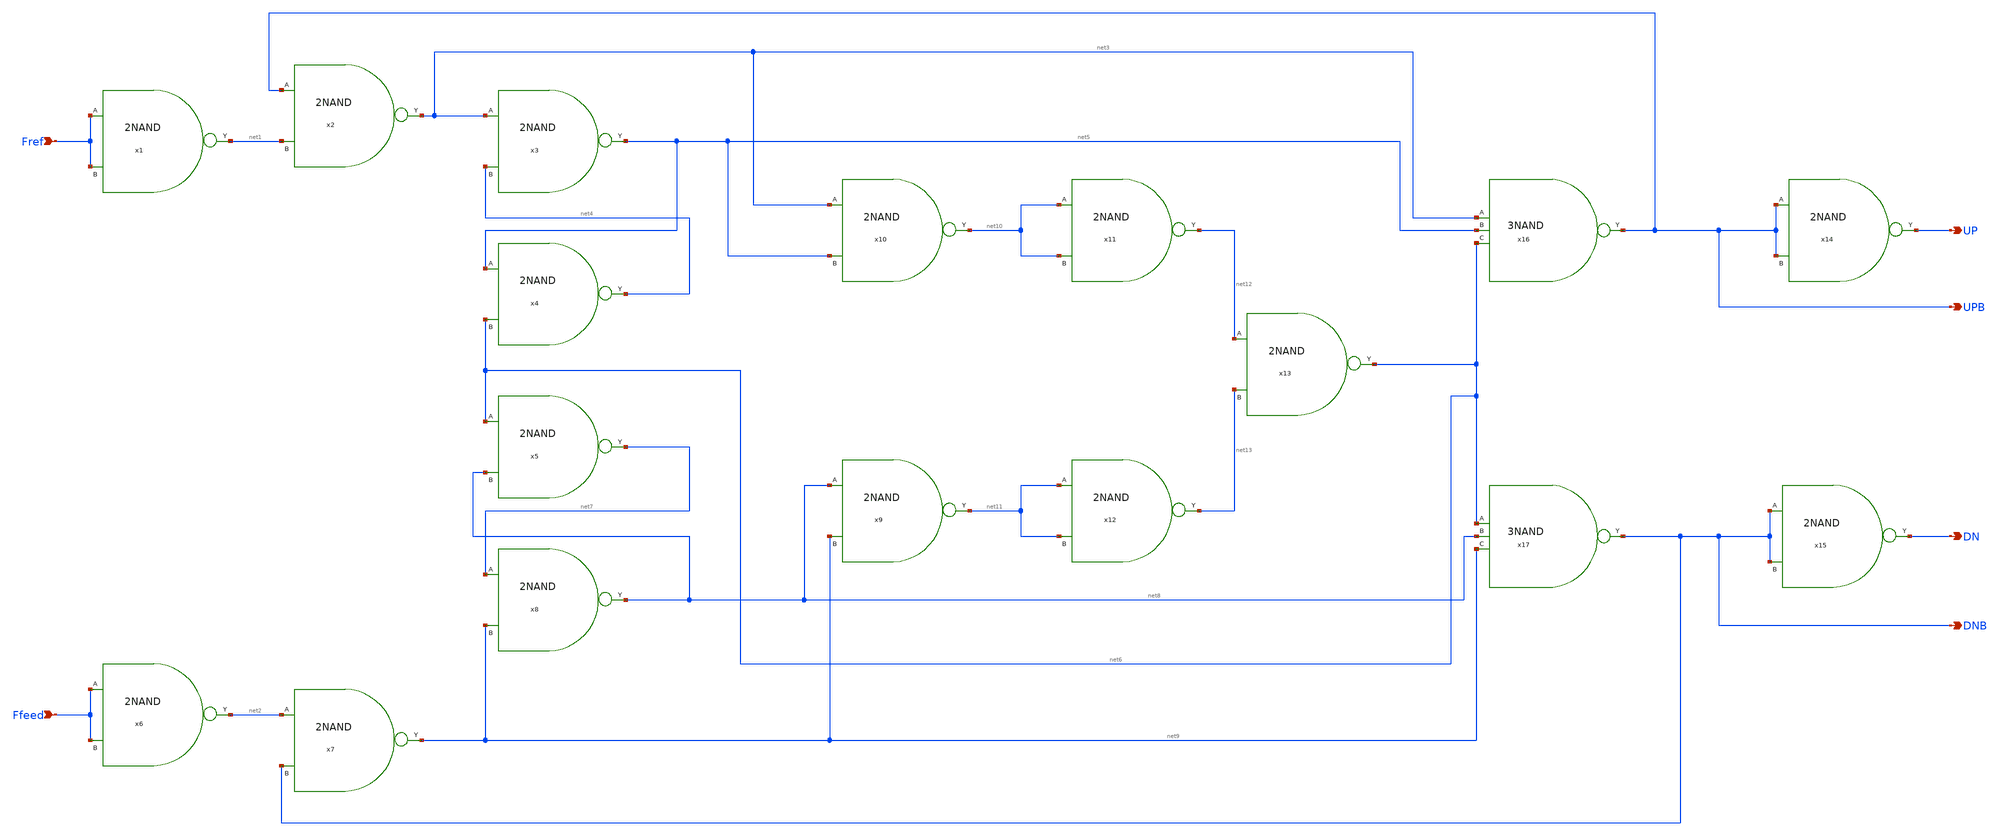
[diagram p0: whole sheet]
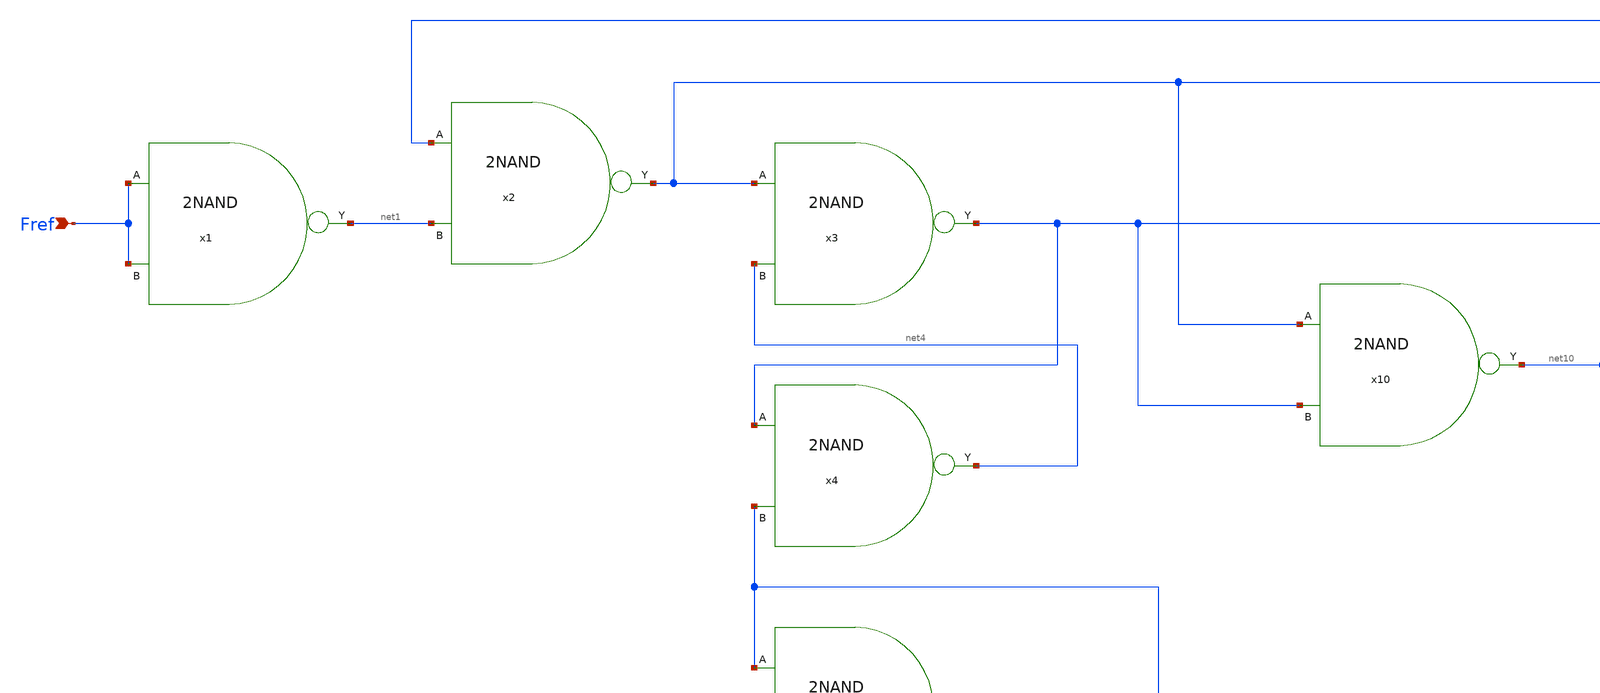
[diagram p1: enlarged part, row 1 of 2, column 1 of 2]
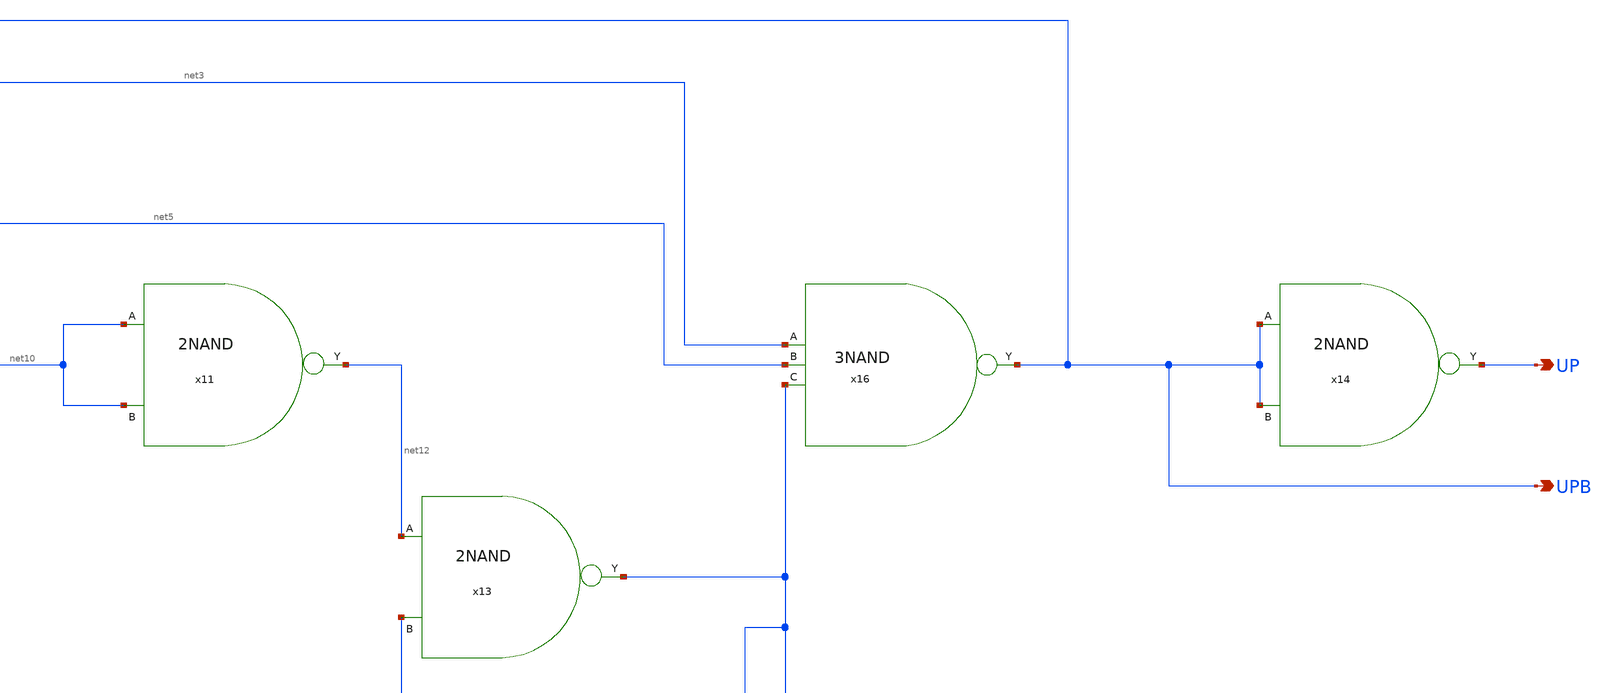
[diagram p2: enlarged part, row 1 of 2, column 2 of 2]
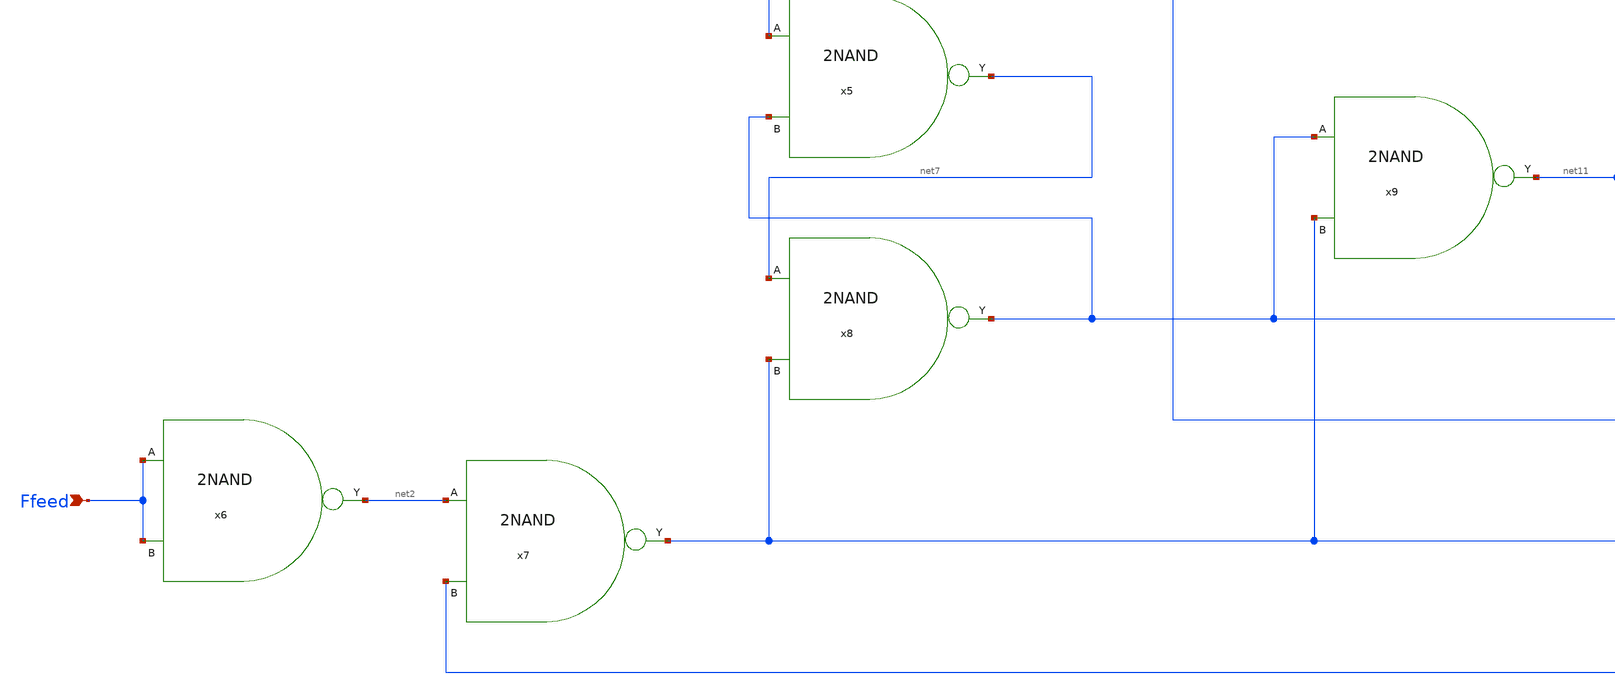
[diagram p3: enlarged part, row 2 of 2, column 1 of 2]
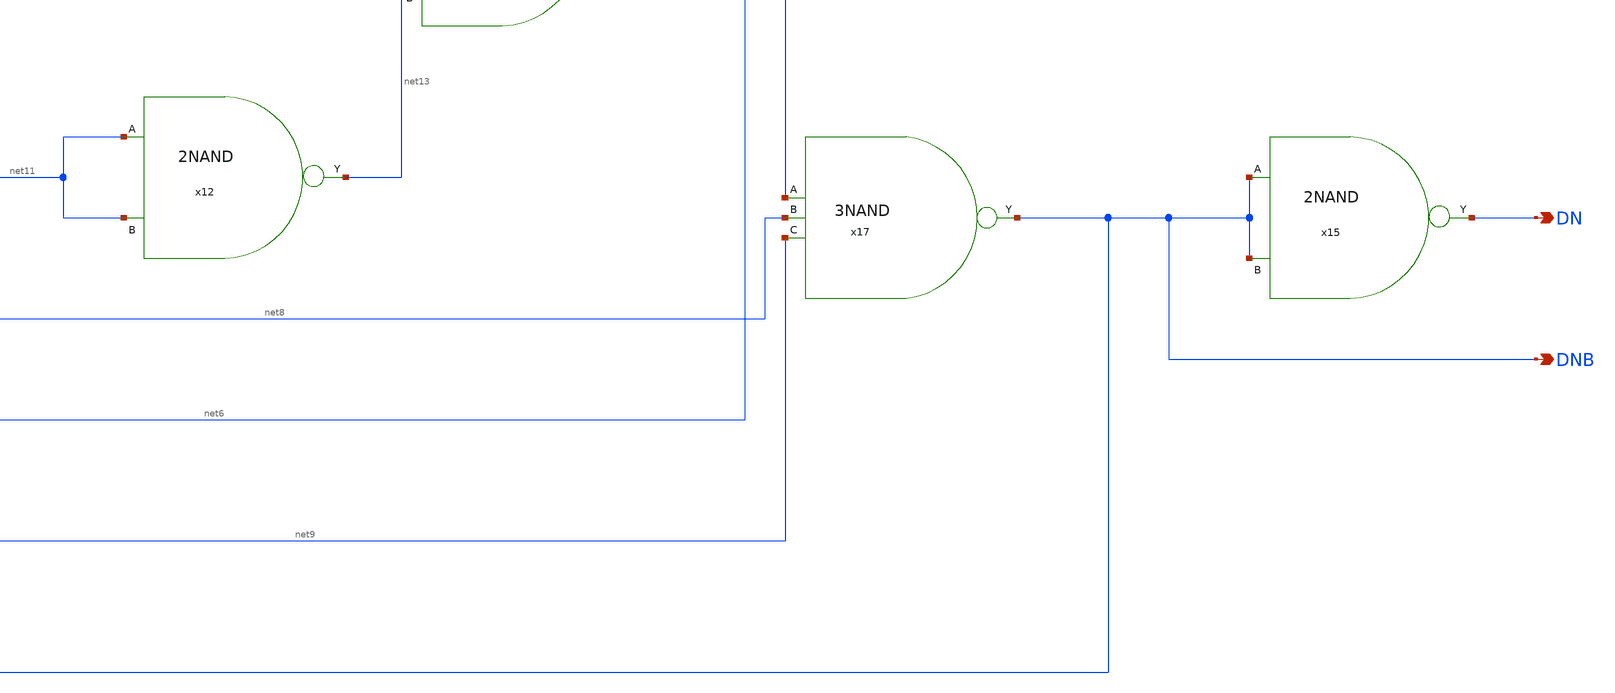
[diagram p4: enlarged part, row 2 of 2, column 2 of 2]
** sch_path: Team 1 Design/design_data/xschem/PFD/PFD.sch
**.subckt PFD Fref Ffeed UP UPB DN DNB
*.ipin Fref
*.ipin Ffeed
*.opin UP
*.opin UPB
*.opin DN
*.opin DNB
x1 Fref net1 Fref 2NAND
x2 UPB net3 net1 2NAND
x3 net3 net5 net4 2NAND
x4 net5 net4 net6 2NAND
x5 net6 net7 net8 2NAND
x6 Ffeed net2 Ffeed 2NAND
x7 net2 net9 DNB 2NAND
x8 net7 net8 net9 2NAND
x9 net8 net11 net9 2NAND
x10 net3 net10 net5 2NAND
x11 net10 net12 net10 2NAND
x12 net11 net13 net11 2NAND
x13 net12 net6 net13 2NAND
x14 UPB UP UPB 2NAND
x15 DNB DN DNB 2NAND
x16 UPB net3 net5 net6 3NAND
x17 DNB net6 net8 net9 3NAND
**.ends

* expanding   symbol:  /foss/designs/Team1/2NAND/2NAND.sym # of pins=3
** sym_path: Team 1 Design/design_data/xschem/2_Input_NAND/2NAND.sym
** sch_path: Team 1 Design/design_data/xschem/2_Input_NAND/2NAND.sch
.subckt 2NAND A Y B
*.ipin B
*.opin Y
*.ipin A
XM1 Y A net1 net1 sg13_lv_pmos w=2u l=0.13u ng=1 m=1 mm_ok=1
XM2 Y B net1 net1 sg13_lv_pmos w=2u l=0.13u ng=1 m=1 mm_ok=1
XM3 Y B net2 GND sg13_lv_nmos w=1u l=0.13u ng=1 m=1 mm_ok=1
XM4 net2 A GND GND sg13_lv_nmos w=1u l=0.13u ng=1 m=1 mm_ok=1
V1 net1 GND 1.2
.ends


* expanding   symbol:  /foss/designs/Team1/3NAND/3NAND.sym # of pins=4
** sym_path: Team 1 Design/design_data/xschem/3_Input_NAND/3NAND.sym
** sch_path: Team 1 Design/design_data/xschem/3_Input_NAND/3NAND.sch
.subckt 3NAND Y A B C
*.ipin A
*.ipin B
*.ipin C
*.opin Y
XM1 Y A Vdd Vdd sg13_lv_pmos w=2u l=0.13u ng=1 m=1 mm_ok=1
XM2 Y B Vdd Vdd sg13_lv_pmos w=2u l=0.13u ng=1 m=1 mm_ok=1
XM3 Y C Vdd Vdd sg13_lv_pmos w=2u l=0.13u ng=1 m=1 mm_ok=1
XM4 Y A net1 GND sg13_lv_nmos w=1u l=0.13u ng=1 m=1 mm_ok=1
XM5 net1 B net2 GND sg13_lv_nmos w=1u l=0.13u ng=1 m=1 mm_ok=1
XM6 net2 C GND GND sg13_lv_nmos w=1u l=0.13u ng=1 m=1 mm_ok=1
V1 Vdd GND 1.2
.ends

.GLOBAL GND
.end
